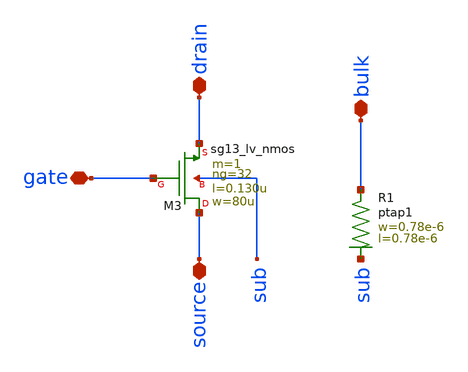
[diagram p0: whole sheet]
** sch_path: ts_pr_May2024/design_data/xschem/nmos32.sch
**.subckt nmos32 drain source bulk gate
*.iopin drain
*.iopin source
*.iopin bulk
*.iopin gate
XR1 bulk sub ptap1 R=262.8 w=0.78e-6 l=0.78e-6
XM3 source gate drain sub sg13_lv_nmos w=80u l=0.130u ng=32 m=1 mm_ok=1
**.ends
.end
